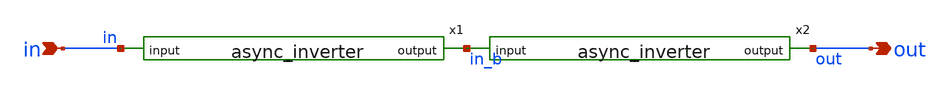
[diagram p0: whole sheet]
** sch_path: xschem/sar_adc/blocks/async_sar/async_buf_strong.sch
**.subckt async_buf_strong in out
*.ipin in
*.opin out
x1 in in_b async_inverter
x2 in_b out async_inverter
**.ends

* expanding   symbol:  sar_adc/blocks/async_sar/async_inverter.sym # of pins=2
** sym_path: xschem/sar_adc/blocks/async_sar/async_inverter.sym
** sch_path: xschem/sar_adc/blocks/async_sar/async_inverter.sch
.subckt async_inverter input out
*.ipin input
*.opin out
XM5 out input VDD VDD pfet_03v3 L=0.28u W=0.80u nf=1 ad='int((nf+1)/2) * W/nf * 0.18u' as='int((nf+2)/2) * W/nf * 0.18u'
+ pd='2*int((nf+1)/2) * (W/nf + 0.18u)' ps='2*int((nf+2)/2) * (W/nf + 0.18u)' nrd='0.18u / W' nrs='0.18u / W'
+ sa=0 sb=0 sd=0 m=1
XM6 out input VSS VSS nfet_03v3 L=0.28u W=0.42u nf=1 ad='int((nf+1)/2) * W/nf * 0.18u' as='int((nf+2)/2) * W/nf * 0.18u'
+ pd='2*int((nf+1)/2) * (W/nf + 0.18u)' ps='2*int((nf+2)/2) * (W/nf + 0.18u)' nrd='0.18u / W' nrs='0.18u / W'
+ sa=0 sb=0 sd=0 m=1
.ends

.end
